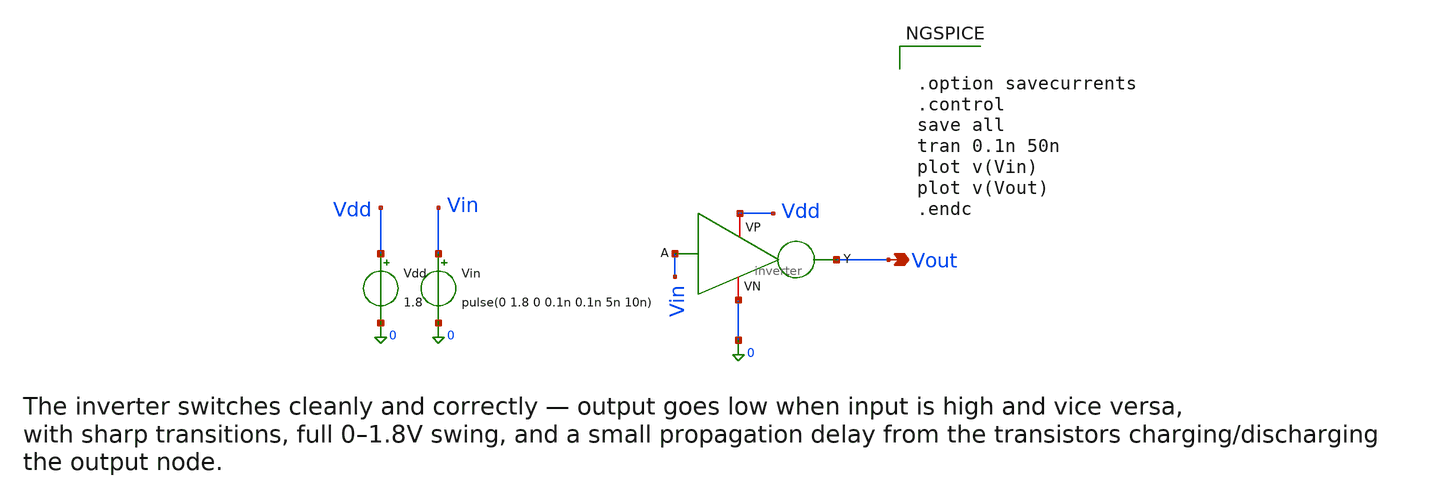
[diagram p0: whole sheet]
** sch_path: Familiarization of open source design flow/Testbench/inverter_tran_tb.sch
**.subckt inverter_tran_tb Vout
*.opin Vout
Vdd Vdd 0 1.8
Vin Vin 0 pulse(0 1.8 0 0.1n 0.1n 5n 10n)
x1 Vdd Vin Vout 0 inverter
**** begin user architecture code

** opencircuitdesign pdks install
.lib $::SKYWATER_MODELS/sky130.lib.spice tt



.option savecurrents
.control
save all
tran 0.1n 50n
plot v(Vin)
plot v(Vout)
.endc


**** end user architecture code
**.ends
.end
